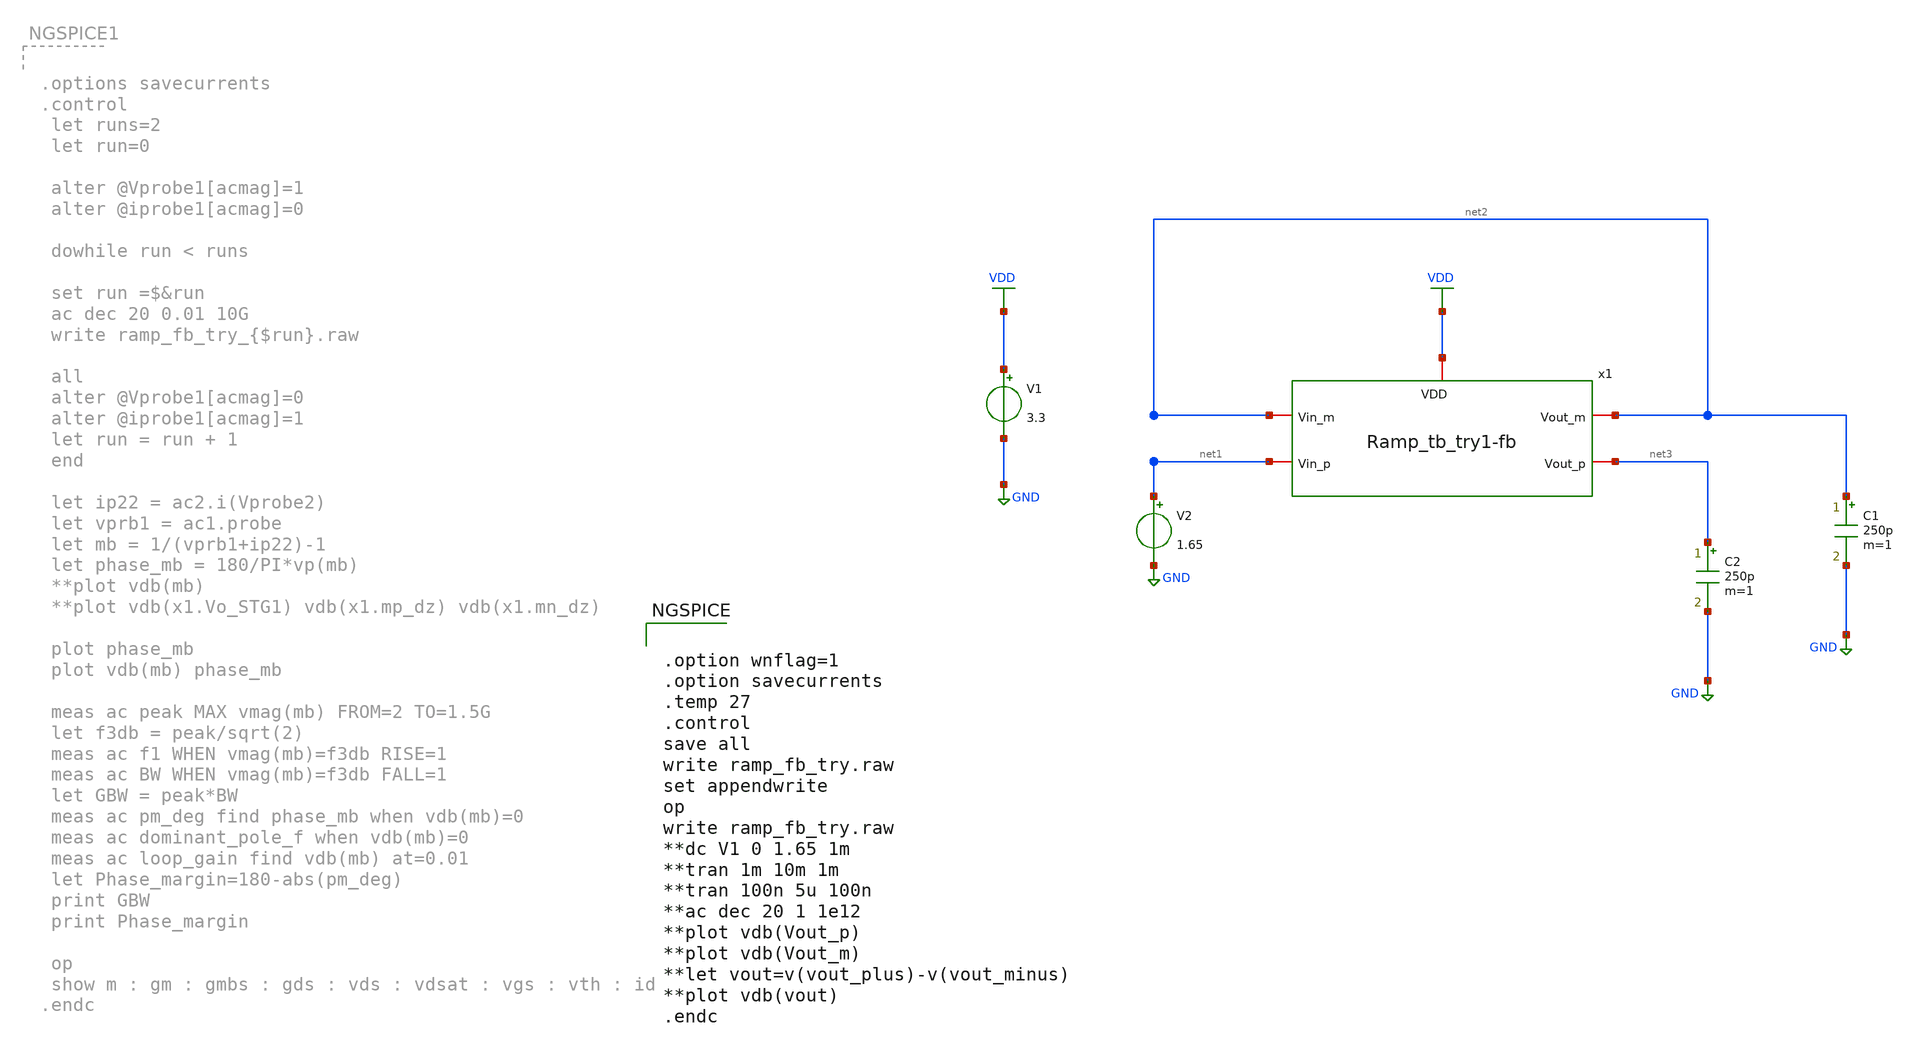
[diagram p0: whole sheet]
** sch_path: Design_Files/Ring-amp/tb/ramp_fb_try.sch
**.subckt ramp_fb_try
x1 VDD net3 net2 net2 net1 Ramp_tb_try1-fb
V1 VDD GND 3.3
V2 net1 GND 1.65
C1 net2 GND 250p m=1
C2 net3 GND 250p m=1
**** begin user architecture code


.save @m.xm1.m0[gm]
.save @m.xm1.m0[id]
.save @m.xm1.m0[vth]
.save @m.xm1.m0[vds]
.save @m.xm1.m0[gds]
.save @m.xm1.m0[cgg]
.save @m.xm1.m0[cgs]
.save @m.xm1.m0[cgd]
.save @m.xm2.m0[gm]
.save @m.xm2.m0[id]
.save @m.xm2.m0[vth]
.save @m.xm2.m0[vds]
.save @m.xm2.m0[gds]
.save @m.xm2.m0[cgg]
.save @m.xm2.m0[cgs]
.save @m.xm2.m0[cgd]
.save @m.xm3.m0[gm]
.save @m.xm3.m0[id]
.save @m.xm3.m0[vth]
.save @m.xm3.m0[vds]
.save @m.xm3.m0[gds]
.save @m.xm3.m0[cgg]
.save @m.xm3.m0[cgs]
.save @m.xm3.m0[cgd]
.save @m.xm4.m0[gm]
.save @m.xm4.m0[id]
.save @m.xm4.m0[vth]
.save @m.xm4.m0[vds]
.save @m.xm4.m0[gds]
.save @m.xm4.m0[cgg]
.save @m.xm4.m0[cgs]
.save @m.xm4.m0[cgd]
.save @m.xm5.m0[gm]
.save @m.xm5.m0[id]
.save @m.xm5.m0[vth]
.save @m.xm5.m0[vds]
.save @m.xm5.m0[gds]
.save @m.xm5.m0[cgg]
.save @m.xm5.m0[cgs]
.save @m.xm5.m0[cgd]
.save @m.xm6.m0[gm]
.save @m.xm6.m0[id]
.save @m.xm6.m0[vth]
.save @m.xm6.m0[vds]
.save @m.xm6.m0[gds]
.save @m.xm6.m0[cgg]
.save @m.xm6.m0[cgs]
.save @m.xm6.m0[cgd]
.save @m.xm7.m0[gm]
.save @m.xm7.m0[id]
.save @m.xm7.m0[vth]
.save @m.xm7.m0[vds]
.save @m.xm7.m0[gds]
.save @m.xm7.m0[cgg]
.save @m.xm7.m0[cgs]
.save @m.xm7.m0[cgd]
.save @m.xm8.m0[gm]
.save @m.xm8.m0[id]
.save @m.xm8.m0[vth]
.save @m.xm8.m0[vds]
.save @m.xm8.m0[gds]
.save @m.xm8.m0[cgg]
.save @m.xm8.m0[cgs]
.save @m.xm8.m0[cgd]
.save @m.xm9.m0[gm]
.save @m.xm9.m0[id]
.save @m.xm9.m0[vth]
.save @m.xm9.m0[vds]
.save @m.xm9.m0[gds]
.save @m.xm9.m0[cgg]
.save @m.xm9.m0[cgs]
.save @m.xm9.m0[cgd]
.save @m.xm10.m0[gm]
.save @m.xm10.m0[id]
.save @m.xm10.m0[vth]
.save @m.xm10.m0[vds]
.save @m.xm10.m0[gds]
.save @m.xm10.m0[cgg]
.save @m.xm10.m0[cgs]
.save @m.xm10.m0[cgd]
.save @m.xm11.m0[gm]
.save @m.xm11.m0[id]
.save @m.xm11.m0[vth]
.save @m.xm11.m0[vds]
.save @m.xm11.m0[gds]
.save @m.xm11.m0[cgg]
.save @m.xm11.m0[cgs]
.save @m.xm11.m0[cgd]
.save @m.xm12.m0[gm]
.save @m.xm12.m0[id]
.save @m.xm12.m0[vth]
.save @m.xm12.m0[vds]
.save @m.xm12.m0[gds]
.save @m.xm12.m0[cgg]
.save @m.xm12.m0[cgs]
.save @m.xm12.m0[cgd]
.save @m.xm13.m0[gm]
.save @m.xm13.m0[id]
.save @m.xm13.m0[vth]
.save @m.xm13.m0[vds]
.save @m.xm13.m0[gds]
.save @m.xm13.m0[cgg]
.save @m.xm13.m0[cgs]
.save @m.xm13.m0[cgd]
.save @m.xm14.m0[gm]
.save @m.xm14.m0[id]
.save @m.xm14.m0[vth]
.save @m.xm14.m0[vds]
.save @m.xm14.m0[gds]
.save @m.xm14.m0[cgg]
.save @m.xm14.m0[cgs]
.save @m.xm14.m0[cgd]
.save @m.xm15.m0[gm]
.save @m.xm15.m0[id]
.save @m.xm15.m0[vth]
.save @m.xm15.m0[vds]
.save @m.xm15.m0[gds]
.save @m.xm15.m0[cgg]
.save @m.xm15.m0[cgs]
.save @m.xm15.m0[cgd]
.save @m.xm16.m0[gm]
.save @m.xm16.m0[id]
.save @m.xm16.m0[vth]
.save @m.xm16.m0[vds]
.save @m.xm16.m0[gds]
.save @m.xm16.m0[cgg]
.save @m.xm16.m0[cgs]
.save @m.xm16.m0[cgd]
.save @m.xm17.m0[gm]
.save @m.xm17.m0[id]
.save @m.xm17.m0[vth]
.save @m.xm17.m0[vds]
.save @m.xm17.m0[gds]
.save @m.xm17.m0[cgg]
.save @m.xm17.m0[cgs]
.save @m.xm17.m0[cgd]
.save @m.xm18.m0[gm]
.save @m.xm18.m0[id]
.save @m.xm18.m0[vth]
.save @m.xm18.m0[vds]
.save @m.xm18.m0[gds]
.save @m.xm18.m0[cgg]
.save @m.xm18.m0[cgs]
.save @m.xm18.m0[cgd]
.save @m.xm19.m0[gm]
.save @m.xm19.m0[id]
.save @m.xm19.m0[vth]
.save @m.xm19.m0[vds]
.save @m.xm19.m0[gds]
.save @m.xm19.m0[cgg]
.save @m.xm19.m0[cgs]
.save @m.xm19.m0[cgd]
.save @m.xm20.m0[gm]
.save @m.xm20.m0[id]
.save @m.xm20.m0[vth]
.save @m.xm20.m0[vds]
.save @m.xm20.m0[gds]
.save @m.xm20.m0[cgg]
.save @m.xm20.m0[cgs]
.save @m.xm20.m0[cgd]
.save @m.xm21.m0[gm]
.save @m.xm21.m0[id]
.save @m.xm21.m0[vth]
.save @m.xm21.m0[vds]
.save @m.xm21.m0[gds]
.save @m.xm21.m0[cgg]
.save @m.xm21.m0[cgs]
.save @m.xm21.m0[cgd]
.save @m.xm22.m0[gm]
.save @m.xm22.m0[id]
.save @m.xm22.m0[vth]
.save @m.xm22.m0[vds]
.save @m.xm22.m0[gds]
.save @m.xm22.m0[cgg]
.save @m.xm22.m0[cgs]
.save @m.xm22.m0[cgd]
.save @m.xm23.m0[gm]
.save @m.xm23.m0[id]
.save @m.xm23.m0[vth]
.save @m.xm23.m0[vds]
.save @m.xm23.m0[gds]
.save @m.xm23.m0[cgg]
.save @m.xm23.m0[cgs]
.save @m.xm23.m0[cgd]
.save @m.xm24.m0[gm]
.save @m.xm24.m0[id]
.save @m.xm24.m0[vth]
.save @m.xm24.m0[vds]
.save @m.xm24.m0[gds]
.save @m.xm24.m0[cgg]
.save @m.xm24.m0[cgs]
.save @m.xm24.m0[cgd]
.save @m.xm25.m0[gm]
.save @m.xm25.m0[id]
.save @m.xm25.m0[vth]
.save @m.xm25.m0[vds]
.save @m.xm25.m0[gds]
.save @m.xm25.m0[cgg]
.save @m.xm25.m0[cgs]
.save @m.xm25.m0[cgd]
.save @m.xm26.m0[gm]
.save @m.xm26.m0[id]
.save @m.xm26.m0[vth]
.save @m.xm26.m0[vds]
.save @m.xm26.m0[gds]
.save @m.xm26.m0[cgg]
.save @m.xm26.m0[cgs]
.save @m.xm26.m0[cgd]
.save @m.xm27.m0[gm]
.save @m.xm27.m0[id]
.save @m.xm27.m0[vth]
.save @m.xm27.m0[vds]
.save @m.xm27.m0[gds]
.save @m.xm27.m0[cgg]
.save @m.xm27.m0[cgs]
.save @m.xm27.m0[cgd]
.save @m.xm28.m0[gm]
.save @m.xm28.m0[id]
.save @m.xm28.m0[vth]
.save @m.xm28.m0[vds]
.save @m.xm28.m0[gds]
.save @m.xm28.m0[cgg]
.save @m.xm28.m0[cgs]
.save @m.xm28.m0[cgd]
.save @m.xm29.m0[gm]
.save @m.xm29.m0[id]
.save @m.xm29.m0[vth]
.save @m.xm29.m0[vds]
.save @m.xm29.m0[gds]
.save @m.xm29.m0[cgg]
.save @m.xm29.m0[cgs]
.save @m.xm29.m0[cgd]
.save @m.xm30.m0[gm]
.save @m.xm30.m0[id]
.save @m.xm30.m0[vth]
.save @m.xm30.m0[vds]
.save @m.xm30.m0[gds]
.save @m.xm30.m0[cgg]
.save @m.xm30.m0[cgs]
.save @m.xm30.m0[cgd]
.save @m.xm31.m0[gm]
.save @m.xm31.m0[id]
.save @m.xm31.m0[vth]
.save @m.xm31.m0[vds]
.save @m.xm31.m0[gds]
.save @m.xm31.m0[cgg]
.save @m.xm31.m0[cgs]
.save @m.xm31.m0[cgd]
.save @m.xm32.m0[gm]
.save @m.xm32.m0[id]
.save @m.xm32.m0[vth]
.save @m.xm32.m0[vds]
.save @m.xm32.m0[gds]
.save @m.xm32.m0[cgg]
.save @m.xm32.m0[cgs]
.save @m.xm32.m0[cgd]
.save @m.xm33.m0[gm]
.save @m.xm33.m0[id]
.save @m.xm33.m0[vth]
.save @m.xm33.m0[vds]
.save @m.xm33.m0[gds]
.save @m.xm33.m0[cgg]
.save @m.xm33.m0[cgs]
.save @m.xm33.m0[cgd]
.save @m.xm34.m0[gm]
.save @m.xm34.m0[id]
.save @m.xm34.m0[vth]
.save @m.xm34.m0[vds]
.save @m.xm34.m0[gds]
.save @m.xm34.m0[cgg]
.save @m.xm34.m0[cgs]
.save @m.xm34.m0[cgd]
.save @m.xm35.m0[gm]
.save @m.xm35.m0[id]
.save @m.xm35.m0[vth]
.save @m.xm35.m0[vds]
.save @m.xm35.m0[gds]
.save @m.xm35.m0[cgg]
.save @m.xm35.m0[cgs]
.save @m.xm35.m0[cgd]
.save @m.xm36.m0[gm]
.save @m.xm36.m0[id]
.save @m.xm36.m0[vth]
.save @m.xm36.m0[vds]
.save @m.xm36.m0[gds]
.save @m.xm36.m0[cgg]
.save @m.xm36.m0[cgs]
.save @m.xm36.m0[cgd]
.save @m.xm37.m0[gm]
.save @m.xm37.m0[id]
.save @m.xm37.m0[vth]
.save @m.xm37.m0[vds]
.save @m.xm37.m0[gds]
.save @m.xm37.m0[cgg]
.save @m.xm37.m0[cgs]
.save @m.xm37.m0[cgd]
.save @m.xm38.m0[gm]
.save @m.xm38.m0[id]
.save @m.xm38.m0[vth]
.save @m.xm38.m0[vds]
.save @m.xm38.m0[gds]
.save @m.xm38.m0[cgg]
.save @m.xm38.m0[cgs]
.save @m.xm38.m0[cgd]



.lib /foss/pdks/volare/gf180mcu/versions/0fe599b2afb6708d281543108caf8310912f54af/gf180mcuD/libs.tech/ngspice/sm141064.ngspice typical
.include /foss/pdks/volare/gf180mcu/versions/0fe599b2afb6708d281543108caf8310912f54af/gf180mcuD/libs.tech/ngspice/design.ngspice
.lib /foss/pdks/volare/gf180mcu/versions/0fe599b2afb6708d281543108caf8310912f54af/gf180mcuD/libs.tech/ngspice/sm141064.ngspice res_statistical

**.include $::180MCU_MODELS/design.ngspice
**.lib $::180MCU_MODELS/sm141064.ngspice typical
**.lib $::180MCU_MODELS/sm141064.ngspice res_typical
* .lib $::180MCU_MODELS/sm141064.ngspice res_statistical
*.include $::180MCU_MODELS/design.ngspice
*.lib $::180MCU_MODELS/sm141064.ngspice typical




.option wnflag=1
.option savecurrents
.temp 27
.control
save all
write ramp_fb_try.raw
set appendwrite
op
write ramp_fb_try.raw
**dc V1 0 1.65 1m
**tran 1m 10m 1m
**tran 100n 5u 100n
**ac dec 20 1 1e12
**plot vdb(Vout_p)
**plot vdb(Vout_m)
**let vout=v(vout_plus)-v(vout_minus)
**plot vdb(vout)
.endc


**** end user architecture code
**.ends
.GLOBAL GND
.GLOBAL VDD
.end
